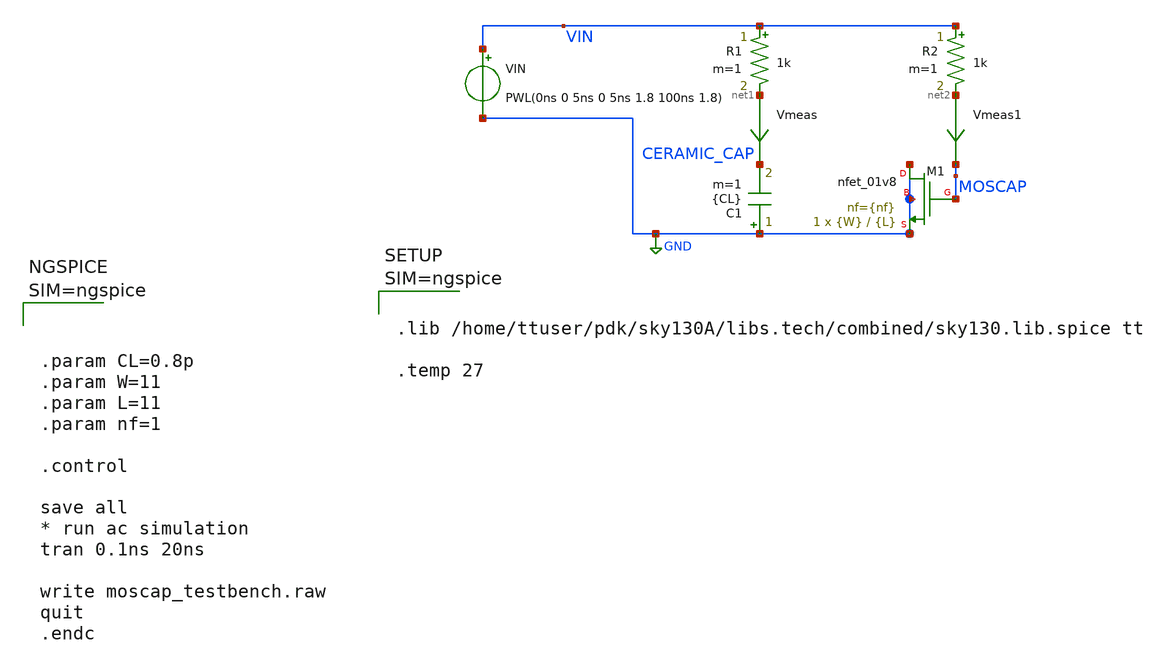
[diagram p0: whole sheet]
** sch_path: xschem/moscap_testbench.sch
**.subckt moscap_testbench
VIN VIN GND PWL(0ns 0 5ns 0 5ns 1.8 100ns 1.8)
R1 VIN net1 1k m=1
R2 VIN net2 1k m=1
Vmeas net1 CERAMIC_CAP 0
.save i(vmeas)
Vmeas1 net2 MOSCAP 0
.save i(vmeas1)
C1 GND CERAMIC_CAP {CL} m=1
XM1 GND MOSCAP GND GND sky130_fd_pr__nfet_01v8 L={L} W={W} nf={nf} ad='int((nf+1)/2) * W/nf * 0.29' as='int((nf+2)/2) * W/nf * 0.29'
+ pd='2*int((nf+1)/2) * (W/nf + 0.29)' ps='2*int((nf+2)/2) * (W/nf + 0.29)' nrd='0.29 / W' nrs='0.29 / W'
+ sa=0 sb=0 sd=0 mult=1 m=1
**** begin user architecture code




.param CL=0.8p
.param W=11
.param L=11
.param nf=1

.control

save all
* run ac simulation
tran 0.1ns 20ns

write moscap_testbench.raw
quit
.endc






.lib /home/ttuser/pdk/sky130A/libs.tech/combined/sky130.lib.spice tt

.temp 27



**** end user architecture code
**.ends
.GLOBAL GND
.end
